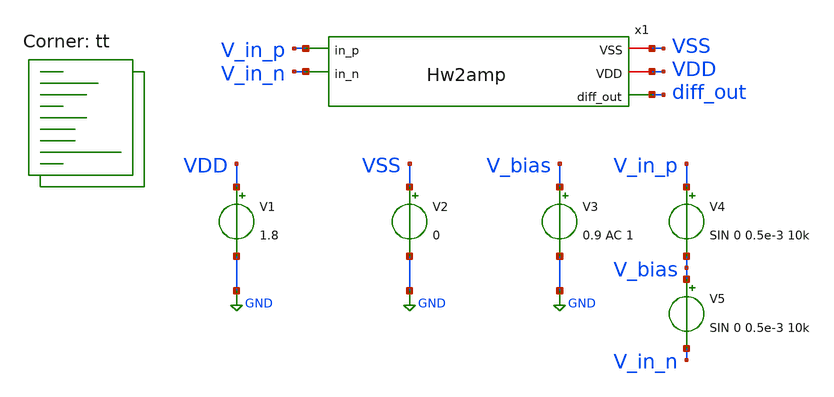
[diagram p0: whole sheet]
** sch_path: xschem/tests/hw2amp_test.sch
**.subckt hw2amp_test
x1 VSS VDD V_in_p V_in_n diff_out Hw2amp
V1 VDD GND 1.8
V2 VSS GND 0
V3 V_bias GND 0.9 AC 1
V4 V_in_p V_bias SIN 0 0.5e-3 10k
V5 V_bias V_in_n SIN 0 0.5e-3 10k
**** begin user architecture code
.lib $::SKYWATER_MODELS/sky130.lib.spice tt



* ngspice commands

.options method=gear
.control
save all
ac dec 20 1 1e6

.endc



**** end user architecture code
**.ends

* expanding   symbol:  src/Hw2amp.sym # of pins=5
** sym_path: xschem/src/Hw2amp.sym
** sch_path: xschem/src/Hw2amp.sch
.subckt Hw2amp VSS VDD in_p in_n diff_out
*.ipin in_p
*.iopin VDD
*.opin diff_out
*.ipin in_n
*.iopin VSS
XM1 net3 VDD VSS VSS sky130_fd_pr__nfet_01v8 L=0.15 W=1 nf=1 ad='int((nf+1)/2) * W/nf * 0.29' as='int((nf+2)/2) * W/nf * 0.29'
+ pd='2*int((nf+1)/2) * (W/nf + 0.29)' ps='2*int((nf+2)/2) * (W/nf + 0.29)' nrd='0.29 / W' nrs='0.29 / W'
+ sa=0 sb=0 sd=0 mult=1 m=1
XM2 net2 net1 VDD VDD sky130_fd_pr__pfet_01v8 L=0.15 W=4.5 nf=1 ad='int((nf+1)/2) * W/nf * 0.29' as='int((nf+2)/2) * W/nf * 0.29'
+ pd='2*int((nf+1)/2) * (W/nf + 0.29)' ps='2*int((nf+2)/2) * (W/nf + 0.29)' nrd='0.29 / W' nrs='0.29 / W'
+ sa=0 sb=0 sd=0 mult=1 m=1
XM3 VDD net1 net1 VDD sky130_fd_pr__pfet_01v8 L=0.15 W=4.5 nf=1 ad='int((nf+1)/2) * W/nf * 0.29' as='int((nf+2)/2) * W/nf * 0.29'
+ pd='2*int((nf+1)/2) * (W/nf + 0.29)' ps='2*int((nf+2)/2) * (W/nf + 0.29)' nrd='0.29 / W' nrs='0.29 / W'
+ sa=0 sb=0 sd=0 mult=1 m=1
XM4 net3 in_n net2 VSS sky130_fd_pr__nfet_01v8 L=0.15 W=4.5 nf=1 ad='int((nf+1)/2) * W/nf * 0.29' as='int((nf+2)/2) * W/nf * 0.29'
+ pd='2*int((nf+1)/2) * (W/nf + 0.29)' ps='2*int((nf+2)/2) * (W/nf + 0.29)' nrd='0.29 / W' nrs='0.29 / W'
+ sa=0 sb=0 sd=0 mult=1 m=1
XM5 net1 in_p net3 VSS sky130_fd_pr__nfet_01v8 L=0.15 W=4.5 nf=1 ad='int((nf+1)/2) * W/nf * 0.29' as='int((nf+2)/2) * W/nf * 0.29'
+ pd='2*int((nf+1)/2) * (W/nf + 0.29)' ps='2*int((nf+2)/2) * (W/nf + 0.29)' nrd='0.29 / W' nrs='0.29 / W'
+ sa=0 sb=0 sd=0 mult=1 m=1
XM6 VSS VDD VDD VSS sky130_fd_pr__nfet_01v8 L=0.15 W=1 nf=1 ad='int((nf+1)/2) * W/nf * 0.29' as='int((nf+2)/2) * W/nf * 0.29'
+ pd='2*int((nf+1)/2) * (W/nf + 0.29)' ps='2*int((nf+2)/2) * (W/nf + 0.29)' nrd='0.29 / W' nrs='0.29 / W'
+ sa=0 sb=0 sd=0 mult=1 m=1
XM7 diff_out net2 VDD VDD sky130_fd_pr__pfet_01v8 L=0.15 W=25.5 nf=1 ad='int((nf+1)/2) * W/nf * 0.29'
+ as='int((nf+2)/2) * W/nf * 0.29' pd='2*int((nf+1)/2) * (W/nf + 0.29)' ps='2*int((nf+2)/2) * (W/nf + 0.29)'
+ nrd='0.29 / W' nrs='0.29 / W' sa=0 sb=0 sd=0 mult=1 m=1
XM8 diff_out VDD VSS VSS sky130_fd_pr__nfet_01v8 L=0.15 W=3 nf=1 ad='int((nf+1)/2) * W/nf * 0.29' as='int((nf+2)/2) * W/nf * 0.29'
+ pd='2*int((nf+1)/2) * (W/nf + 0.29)' ps='2*int((nf+2)/2) * (W/nf + 0.29)' nrd='0.29 / W' nrs='0.29 / W'
+ sa=0 sb=0 sd=0 mult=1 m=1
**** begin user architecture code


**** end user architecture code
.ends

.GLOBAL GND
.end
